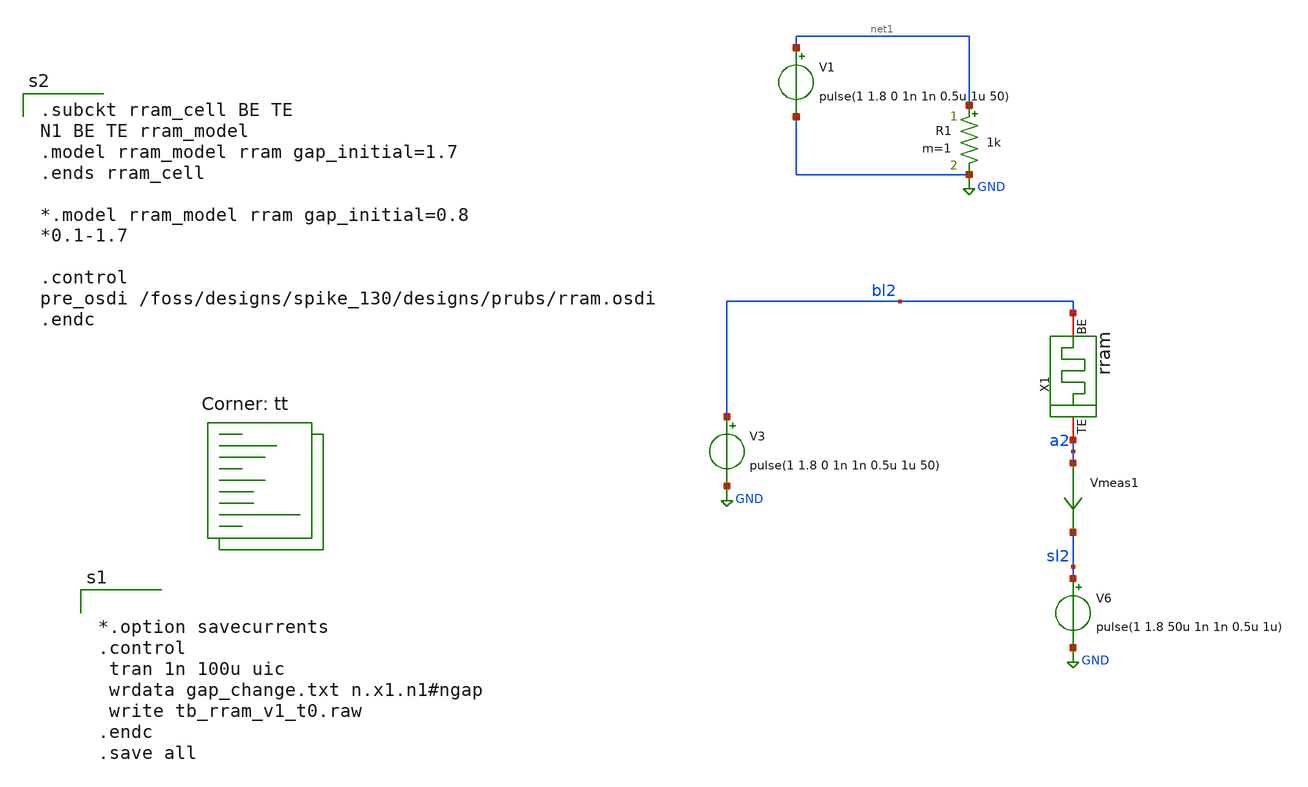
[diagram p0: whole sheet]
** sch_path: designs/tb_memristor/tb_rram_v1_t0.sch
**.subckt tb_rram_v1_t0
V3 bl2 GND pulse(1 1.8 0 1n 1n 0.5u 1u 50)
V6 sl2 GND pulse(1 1.8 50u 1n 1n 0.5u 1u)
Vmeas1 a2 sl2 0
.save i(vmeas1)
X1 a2 bl2 rram_cell
R1 net1 GND 1k m=1
V1 net1 GND pulse(1 1.8 0 1n 1n 0.5u 1u 50)
**** begin user architecture code
.lib $::SKYWATER_MODELS/sky130.lib.spice tt


*.option savecurrents
.control
 tran 1n 100u uic
 wrdata gap_change.txt n.x1.n1#ngap
 write tb_rram_v1_t0.raw
.endc
.save all


.subckt rram_cell BE TE
N1 BE TE rram_model
.model rram_model rram gap_initial=1.7
.ends rram_cell

*.model rram_model rram gap_initial=0.8
*0.1-1.7

.control
pre_osdi /foss/designs/spike_130/designs/prubs/rram.osdi
.endc

**** end user architecture code
**.ends
.GLOBAL GND
.end
